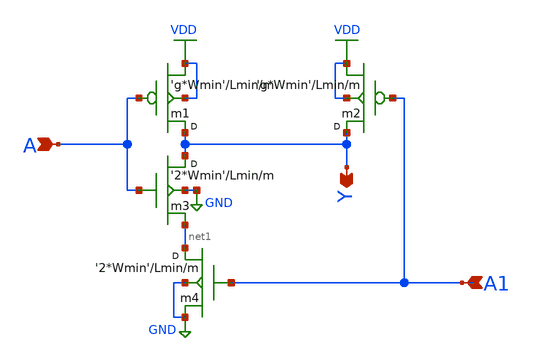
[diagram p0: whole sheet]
** sch_path: Sources/crafted/nand2.sch
**.subckt nand2 A Y A1
*.ipin A
*.opin Y
*.ipin A1
m3 Y A net1 GND nmos4 w='2*Wmin' l=Lmin m=m
m1 Y A VDD VDD pmos4 w='g*Wmin' l=Lmin m=m
m4 net1 A1 GND GND nmos4 w='2*Wmin' l=Lmin m=m
m2 Y A1 VDD VDD pmos4 w='g*Wmin' l=Lmin m=m
**.ends
.GLOBAL VDD
.GLOBAL GND
.end
